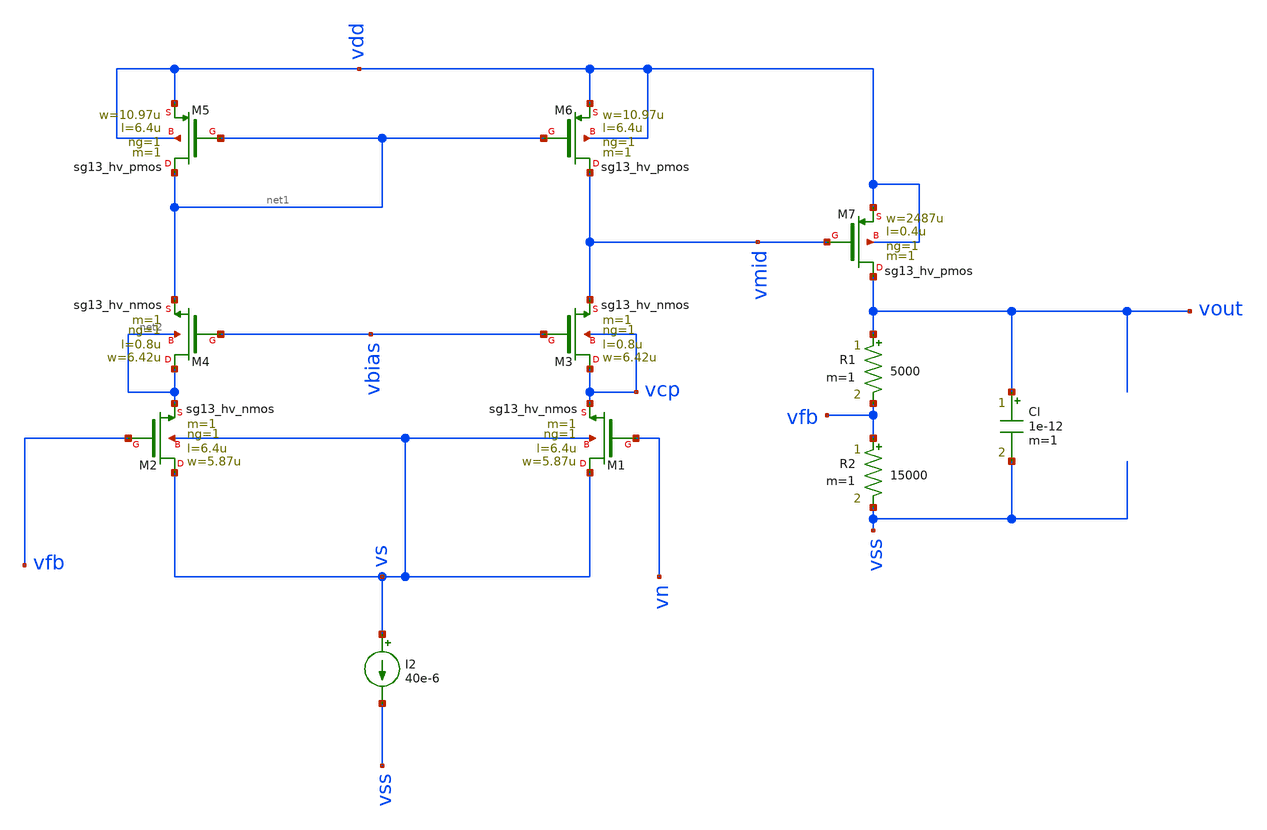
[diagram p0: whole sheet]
** sch_path: test/Tesis_notebooks/xschem/ldo_sim_ihp_cc.sch
**.subckt ldo_sim_ihp_cc
R1 vout vfb 5000 m=1
R2 vfb vss 15000 m=1
Cl vout vss 1e-12 m=1
XM6 vmid net1 vdd vdd sg13_hv_pmos w=10.97u l=6.4u ng=1 m=1 mm_ok=1
I2 vs vss 40e-6
XM1 vs vn vcp vs sg13_hv_nmos w=5.87u l=6.4u ng=1 m=1 mm_ok=1
XM2 vs vfb net2 vs sg13_hv_nmos w=5.87u l=6.4u ng=1 m=1 mm_ok=1
XM3 vcp vbias vmid vcp sg13_hv_nmos w=6.42u l=0.8u ng=1 m=1 mm_ok=1
XM4 net2 vbias net1 net2 sg13_hv_nmos w=6.42u l=0.8u ng=1 m=1 mm_ok=1
XM5 net1 net1 vdd vdd sg13_hv_pmos w=10.97u l=6.4u ng=1 m=1 mm_ok=1
XM7 vout vmid vdd vdd sg13_hv_pmos w=2487u l=0.4u ng=1 m=1 mm_ok=1
**** begin user architecture code



.lib /opt/pdks/ihp-sg13g2/libs.tech/ngspice/models/cornerMOShv.lib mos_tt

Vref vn 0 1.35
Vdd vdd 0 3.3 ac 1
Vss vss 0 0
Vbias vbias 0 2.2

.control
ac dec 10 1 100G
plot vdb(vout)
plot phase(vout)
op
print vout vmid vcp vfb vs
.endc



**** end user architecture code
**.ends
.end
